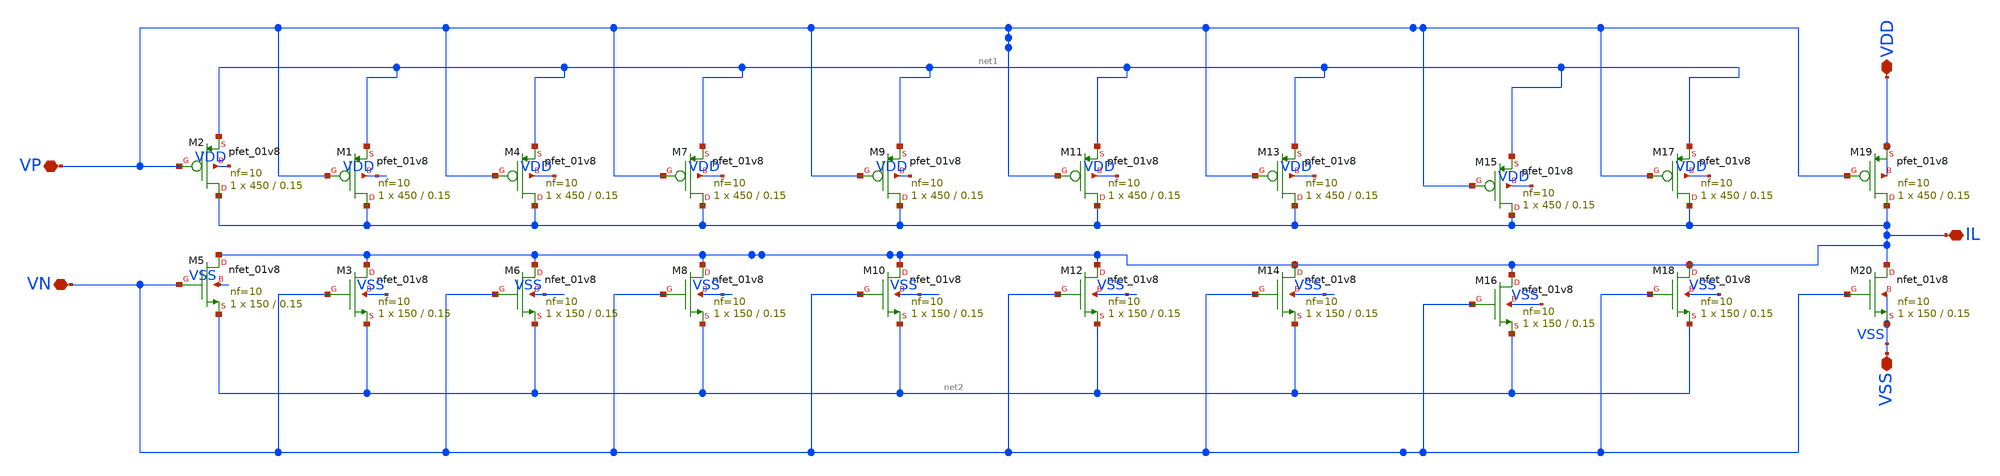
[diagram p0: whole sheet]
** sch_path: xschem/DC_DC_Converter_xschem/Power_mosfets.sch
**.subckt Power_mosfets VDD VSS VP VN IL
*.iopin VDD
*.iopin VSS
*.iopin VP
*.iopin VN
*.iopin IL
XM2 IL VP net1 VDD sky130_fd_pr__pfet_01v8 L=0.15 W=450 nf=10 ad='int((nf+1)/2) * W/nf * 0.29' as='int((nf+2)/2) * W/nf * 0.29'
+ pd='2*int((nf+1)/2) * (W/nf + 0.29)' ps='2*int((nf+2)/2) * (W/nf + 0.29)' nrd='0.29 / W' nrs='0.29 / W'
+ sa=0 sb=0 sd=0 mult=1 m=1
XM5 IL VN net2 VSS sky130_fd_pr__nfet_01v8 L=0.15 W=150 nf=10 ad='int((nf+1)/2) * W/nf * 0.29' as='int((nf+2)/2) * W/nf * 0.29'
+ pd='2*int((nf+1)/2) * (W/nf + 0.29)' ps='2*int((nf+2)/2) * (W/nf + 0.29)' nrd='0.29 / W' nrs='0.29 / W'
+ sa=0 sb=0 sd=0 mult=1 m=1
XM1 IL VP net1 VDD sky130_fd_pr__pfet_01v8 L=0.15 W=450 nf=10 ad='int((nf+1)/2) * W/nf * 0.29' as='int((nf+2)/2) * W/nf * 0.29'
+ pd='2*int((nf+1)/2) * (W/nf + 0.29)' ps='2*int((nf+2)/2) * (W/nf + 0.29)' nrd='0.29 / W' nrs='0.29 / W'
+ sa=0 sb=0 sd=0 mult=1 m=1
XM3 IL VN net2 VSS sky130_fd_pr__nfet_01v8 L=0.15 W=150 nf=10 ad='int((nf+1)/2) * W/nf * 0.29' as='int((nf+2)/2) * W/nf * 0.29'
+ pd='2*int((nf+1)/2) * (W/nf + 0.29)' ps='2*int((nf+2)/2) * (W/nf + 0.29)' nrd='0.29 / W' nrs='0.29 / W'
+ sa=0 sb=0 sd=0 mult=1 m=1
XM4 IL VP net1 VDD sky130_fd_pr__pfet_01v8 L=0.15 W=450 nf=10 ad='int((nf+1)/2) * W/nf * 0.29' as='int((nf+2)/2) * W/nf * 0.29'
+ pd='2*int((nf+1)/2) * (W/nf + 0.29)' ps='2*int((nf+2)/2) * (W/nf + 0.29)' nrd='0.29 / W' nrs='0.29 / W'
+ sa=0 sb=0 sd=0 mult=1 m=1
XM6 IL VN net2 VSS sky130_fd_pr__nfet_01v8 L=0.15 W=150 nf=10 ad='int((nf+1)/2) * W/nf * 0.29' as='int((nf+2)/2) * W/nf * 0.29'
+ pd='2*int((nf+1)/2) * (W/nf + 0.29)' ps='2*int((nf+2)/2) * (W/nf + 0.29)' nrd='0.29 / W' nrs='0.29 / W'
+ sa=0 sb=0 sd=0 mult=1 m=1
XM7 IL VP net1 VDD sky130_fd_pr__pfet_01v8 L=0.15 W=450 nf=10 ad='int((nf+1)/2) * W/nf * 0.29' as='int((nf+2)/2) * W/nf * 0.29'
+ pd='2*int((nf+1)/2) * (W/nf + 0.29)' ps='2*int((nf+2)/2) * (W/nf + 0.29)' nrd='0.29 / W' nrs='0.29 / W'
+ sa=0 sb=0 sd=0 mult=1 m=1
XM8 IL VN net2 VSS sky130_fd_pr__nfet_01v8 L=0.15 W=150 nf=10 ad='int((nf+1)/2) * W/nf * 0.29' as='int((nf+2)/2) * W/nf * 0.29'
+ pd='2*int((nf+1)/2) * (W/nf + 0.29)' ps='2*int((nf+2)/2) * (W/nf + 0.29)' nrd='0.29 / W' nrs='0.29 / W'
+ sa=0 sb=0 sd=0 mult=1 m=1
XM9 IL VP net1 VDD sky130_fd_pr__pfet_01v8 L=0.15 W=450 nf=10 ad='int((nf+1)/2) * W/nf * 0.29' as='int((nf+2)/2) * W/nf * 0.29'
+ pd='2*int((nf+1)/2) * (W/nf + 0.29)' ps='2*int((nf+2)/2) * (W/nf + 0.29)' nrd='0.29 / W' nrs='0.29 / W'
+ sa=0 sb=0 sd=0 mult=1 m=1
XM10 IL VN net2 VSS sky130_fd_pr__nfet_01v8 L=0.15 W=150 nf=10 ad='int((nf+1)/2) * W/nf * 0.29' as='int((nf+2)/2) * W/nf * 0.29'
+ pd='2*int((nf+1)/2) * (W/nf + 0.29)' ps='2*int((nf+2)/2) * (W/nf + 0.29)' nrd='0.29 / W' nrs='0.29 / W'
+ sa=0 sb=0 sd=0 mult=1 m=1
XM11 IL VP net1 VDD sky130_fd_pr__pfet_01v8 L=0.15 W=450 nf=10 ad='int((nf+1)/2) * W/nf * 0.29' as='int((nf+2)/2) * W/nf * 0.29'
+ pd='2*int((nf+1)/2) * (W/nf + 0.29)' ps='2*int((nf+2)/2) * (W/nf + 0.29)' nrd='0.29 / W' nrs='0.29 / W'
+ sa=0 sb=0 sd=0 mult=1 m=1
XM12 IL VN net2 VSS sky130_fd_pr__nfet_01v8 L=0.15 W=150 nf=10 ad='int((nf+1)/2) * W/nf * 0.29' as='int((nf+2)/2) * W/nf * 0.29'
+ pd='2*int((nf+1)/2) * (W/nf + 0.29)' ps='2*int((nf+2)/2) * (W/nf + 0.29)' nrd='0.29 / W' nrs='0.29 / W'
+ sa=0 sb=0 sd=0 mult=1 m=1
XM13 IL VP net1 VDD sky130_fd_pr__pfet_01v8 L=0.15 W=450 nf=10 ad='int((nf+1)/2) * W/nf * 0.29' as='int((nf+2)/2) * W/nf * 0.29'
+ pd='2*int((nf+1)/2) * (W/nf + 0.29)' ps='2*int((nf+2)/2) * (W/nf + 0.29)' nrd='0.29 / W' nrs='0.29 / W'
+ sa=0 sb=0 sd=0 mult=1 m=1
XM14 IL VN net2 VSS sky130_fd_pr__nfet_01v8 L=0.15 W=150 nf=10 ad='int((nf+1)/2) * W/nf * 0.29' as='int((nf+2)/2) * W/nf * 0.29'
+ pd='2*int((nf+1)/2) * (W/nf + 0.29)' ps='2*int((nf+2)/2) * (W/nf + 0.29)' nrd='0.29 / W' nrs='0.29 / W'
+ sa=0 sb=0 sd=0 mult=1 m=1
XM15 IL VP net1 VDD sky130_fd_pr__pfet_01v8 L=0.15 W=450 nf=10 ad='int((nf+1)/2) * W/nf * 0.29' as='int((nf+2)/2) * W/nf * 0.29'
+ pd='2*int((nf+1)/2) * (W/nf + 0.29)' ps='2*int((nf+2)/2) * (W/nf + 0.29)' nrd='0.29 / W' nrs='0.29 / W'
+ sa=0 sb=0 sd=0 mult=1 m=1
XM16 IL VN net2 VSS sky130_fd_pr__nfet_01v8 L=0.15 W=150 nf=10 ad='int((nf+1)/2) * W/nf * 0.29' as='int((nf+2)/2) * W/nf * 0.29'
+ pd='2*int((nf+1)/2) * (W/nf + 0.29)' ps='2*int((nf+2)/2) * (W/nf + 0.29)' nrd='0.29 / W' nrs='0.29 / W'
+ sa=0 sb=0 sd=0 mult=1 m=1
XM17 IL VP net1 VDD sky130_fd_pr__pfet_01v8 L=0.15 W=450 nf=10 ad='int((nf+1)/2) * W/nf * 0.29' as='int((nf+2)/2) * W/nf * 0.29'
+ pd='2*int((nf+1)/2) * (W/nf + 0.29)' ps='2*int((nf+2)/2) * (W/nf + 0.29)' nrd='0.29 / W' nrs='0.29 / W'
+ sa=0 sb=0 sd=0 mult=1 m=1
XM18 IL VN net2 VSS sky130_fd_pr__nfet_01v8 L=0.15 W=150 nf=10 ad='int((nf+1)/2) * W/nf * 0.29' as='int((nf+2)/2) * W/nf * 0.29'
+ pd='2*int((nf+1)/2) * (W/nf + 0.29)' ps='2*int((nf+2)/2) * (W/nf + 0.29)' nrd='0.29 / W' nrs='0.29 / W'
+ sa=0 sb=0 sd=0 mult=1 m=1
XM19 IL VP VDD VDD sky130_fd_pr__pfet_01v8 L=0.15 W=450 nf=10 ad='int((nf+1)/2) * W/nf * 0.29' as='int((nf+2)/2) * W/nf * 0.29'
+ pd='2*int((nf+1)/2) * (W/nf + 0.29)' ps='2*int((nf+2)/2) * (W/nf + 0.29)' nrd='0.29 / W' nrs='0.29 / W'
+ sa=0 sb=0 sd=0 mult=1 m=1
XM20 IL VN VSS VSS sky130_fd_pr__nfet_01v8 L=0.15 W=150 nf=10 ad='int((nf+1)/2) * W/nf * 0.29' as='int((nf+2)/2) * W/nf * 0.29'
+ pd='2*int((nf+1)/2) * (W/nf + 0.29)' ps='2*int((nf+2)/2) * (W/nf + 0.29)' nrd='0.29 / W' nrs='0.29 / W'
+ sa=0 sb=0 sd=0 mult=1 m=1
**.ends
.end
